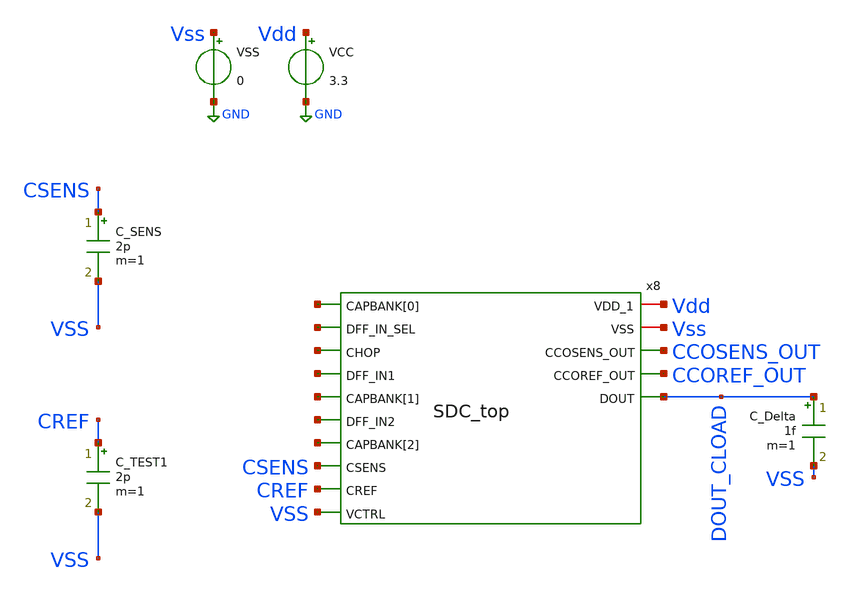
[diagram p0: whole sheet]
** sch_path: ABC123_SDC/design_data/xschem/top/tb_top.sch
**.subckt tb_top
VCC Vdd GND 3.3
VSS Vss GND 0
x8 net1 net2 net3 Vdd net4 net5 Vss net6 net7 CCOSENS_OUT CCOREF_OUT DOUT_CLOAD CSENS CREF VSS
+ SDC_top
C_SENS CSENS VSS 2p m=1
C_TEST1 CREF VSS 2p m=1
C_Delta DOUT_CLOAD VSS 1f m=1
**** begin user architecture code


.ic v(v_si) = 3.3
.ic v(v_ri) = 0
.save v(DOUT_CLOAD) i(VCC)
*.OPTION CSHUNT=0.01e-12
.OPTION ABSTOL=1e-15.
.OPTION GMIN=1.0e-12.
.OPTION ITL1=1e5
.OPTION RSHUNT=1e12
.OPTION RELTOL=1e-5

.option TEMP=27
.control
compose vin_var start=2p stop=5.02p step=0.2p
*compose vin_var start=2p stop=2p step=0.2p
foreach val $&vin_var
  alter C_SENS $val
  save v(DOUT_CLOAD)
  *tran 1n 500u 200u
  tran 1n 50u 20u
  run
end
wrdata /foss/designs/SSCS-Chipathon-2026_ABC123-team/sim_data/data_SDC_CSWEEP.txt
+ tran1.v(DOUT_CLOAD) tran2.v(DOUT_CLOAD) tran3.v(DOUT_CLOAD) tran4.v(DOUT_CLOAD) tran5.v(DOUT_CLOAD) tran6.v(DOUT_CLOAD)
+ tran7.v(DOUT_CLOAD) tran8.v(DOUT_CLOAD) tran9.v(DOUT_CLOAD) tran10.v(DOUT_CLOAD) tran11.v(DOUT_CLOAD)
+ tran12.v(DOUT_CLOAD) tran13.v(DOUT_CLOAD) tran14.v(DOUT_CLOAD) tran15.v(DOUT_CLOAD) tran16.v(DOUT_CLOAD)
wrdata /foss/designs/SSCS-Chipathon-2026_ABC123-team/sim_data/data_SDC_PWR.txt tran16.i(VCC)
rusage time totalcputime
rusage everything > sim_stats.log
.endc



.include $::180MCU_MODELS/design.ngspice
.lib $::180MCU_MODELS/sm141064.ngspice typical
.lib $::180MCU_MODELS/sm141064.ngspice cap_mim
.lib $::180MCU_MODELS/sm141064.ngspice res_typical
.lib $::180MCU_MODELS/sm141064.ngspice moscap_typical
.lib $::180MCU_MODELS/sm141064.ngspice mimcap_typical
* .lib $::180MCU_MODELS/sm141064.ngspice res_statistical

**** end user architecture code
**.ends
.GLOBAL GND
.end
